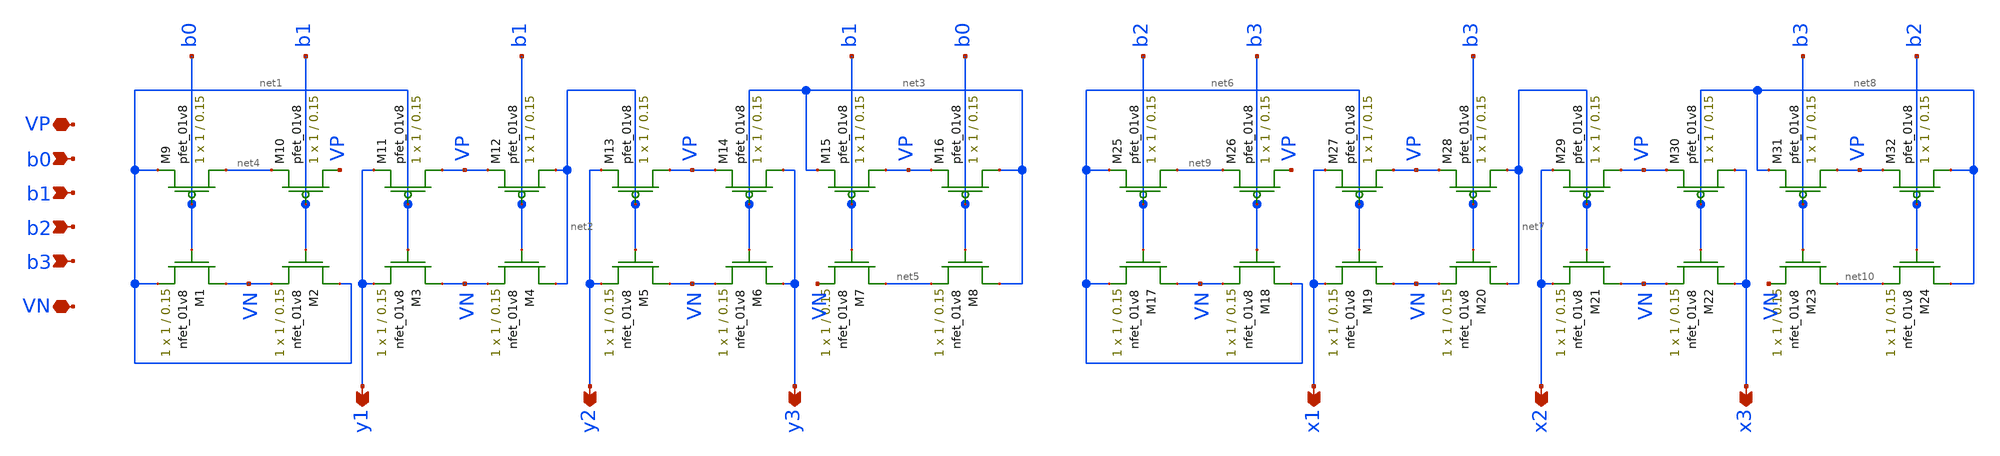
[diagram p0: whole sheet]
** sch_path: xschem/binary_decoder_4bit_lvs.sch
**.subckt binary_decoder_4bit_lvs b0 b1 b2 b3 x3 VP VN y1 y2 y3 x1 x2
*.ipin b0
*.ipin b1
*.ipin b2
*.ipin b3
*.opin x3
*.iopin VP
*.iopin VN
*.opin y1
*.opin y2
*.opin y3
*.opin x1
*.opin x2
XM1 VN b0 net1 GND sky130_fd_pr__nfet_01v8 L=0.15 W=1 nf=1 ad='int((nf+1)/2) * W/nf * 0.29' as='int((nf+2)/2) * W/nf * 0.29'
+ pd='2*int((nf+1)/2) * (W/nf + 0.29)' ps='2*int((nf+2)/2) * (W/nf + 0.29)' nrd='0.29 / W' nrs='0.29 / W'
+ sa=0 sb=0 sd=0 mult=1 m=1
XM2 net1 b1 VN GND sky130_fd_pr__nfet_01v8 L=0.15 W=1 nf=1 ad='int((nf+1)/2) * W/nf * 0.29' as='int((nf+2)/2) * W/nf * 0.29'
+ pd='2*int((nf+1)/2) * (W/nf + 0.29)' ps='2*int((nf+2)/2) * (W/nf + 0.29)' nrd='0.29 / W' nrs='0.29 / W'
+ sa=0 sb=0 sd=0 mult=1 m=1
XM3 VN net1 y1 GND sky130_fd_pr__nfet_01v8 L=0.15 W=1 nf=1 ad='int((nf+1)/2) * W/nf * 0.29' as='int((nf+2)/2) * W/nf * 0.29'
+ pd='2*int((nf+1)/2) * (W/nf + 0.29)' ps='2*int((nf+2)/2) * (W/nf + 0.29)' nrd='0.29 / W' nrs='0.29 / W'
+ sa=0 sb=0 sd=0 mult=1 m=1
XM4 net2 b1 VN GND sky130_fd_pr__nfet_01v8 L=0.15 W=1 nf=1 ad='int((nf+1)/2) * W/nf * 0.29' as='int((nf+2)/2) * W/nf * 0.29'
+ pd='2*int((nf+1)/2) * (W/nf + 0.29)' ps='2*int((nf+2)/2) * (W/nf + 0.29)' nrd='0.29 / W' nrs='0.29 / W'
+ sa=0 sb=0 sd=0 mult=1 m=1
XM5 VN net2 y2 GND sky130_fd_pr__nfet_01v8 L=0.15 W=1 nf=1 ad='int((nf+1)/2) * W/nf * 0.29' as='int((nf+2)/2) * W/nf * 0.29'
+ pd='2*int((nf+1)/2) * (W/nf + 0.29)' ps='2*int((nf+2)/2) * (W/nf + 0.29)' nrd='0.29 / W' nrs='0.29 / W'
+ sa=0 sb=0 sd=0 mult=1 m=1
XM6 y3 net3 VN GND sky130_fd_pr__nfet_01v8 L=0.15 W=1 nf=1 ad='int((nf+1)/2) * W/nf * 0.29' as='int((nf+2)/2) * W/nf * 0.29'
+ pd='2*int((nf+1)/2) * (W/nf + 0.29)' ps='2*int((nf+2)/2) * (W/nf + 0.29)' nrd='0.29 / W' nrs='0.29 / W'
+ sa=0 sb=0 sd=0 mult=1 m=1
XM7 net5 b1 VN GND sky130_fd_pr__nfet_01v8 L=0.15 W=1 nf=1 ad='int((nf+1)/2) * W/nf * 0.29' as='int((nf+2)/2) * W/nf * 0.29'
+ pd='2*int((nf+1)/2) * (W/nf + 0.29)' ps='2*int((nf+2)/2) * (W/nf + 0.29)' nrd='0.29 / W' nrs='0.29 / W'
+ sa=0 sb=0 sd=0 mult=1 m=1
XM8 net3 b0 net5 GND sky130_fd_pr__nfet_01v8 L=0.15 W=1 nf=1 ad='int((nf+1)/2) * W/nf * 0.29' as='int((nf+2)/2) * W/nf * 0.29'
+ pd='2*int((nf+1)/2) * (W/nf + 0.29)' ps='2*int((nf+2)/2) * (W/nf + 0.29)' nrd='0.29 / W' nrs='0.29 / W'
+ sa=0 sb=0 sd=0 mult=1 m=1
XM9 net4 b0 net1 VDD sky130_fd_pr__pfet_01v8 L=0.15 W=1 nf=1 ad='int((nf+1)/2) * W/nf * 0.29' as='int((nf+2)/2) * W/nf * 0.29'
+ pd='2*int((nf+1)/2) * (W/nf + 0.29)' ps='2*int((nf+2)/2) * (W/nf + 0.29)' nrd='0.29 / W' nrs='0.29 / W'
+ sa=0 sb=0 sd=0 mult=1 m=1
XM10 VP b1 net4 VDD sky130_fd_pr__pfet_01v8 L=0.15 W=1 nf=1 ad='int((nf+1)/2) * W/nf * 0.29' as='int((nf+2)/2) * W/nf * 0.29'
+ pd='2*int((nf+1)/2) * (W/nf + 0.29)' ps='2*int((nf+2)/2) * (W/nf + 0.29)' nrd='0.29 / W' nrs='0.29 / W'
+ sa=0 sb=0 sd=0 mult=1 m=1
XM11 VP net1 y1 VDD sky130_fd_pr__pfet_01v8 L=0.15 W=1 nf=1 ad='int((nf+1)/2) * W/nf * 0.29' as='int((nf+2)/2) * W/nf * 0.29'
+ pd='2*int((nf+1)/2) * (W/nf + 0.29)' ps='2*int((nf+2)/2) * (W/nf + 0.29)' nrd='0.29 / W' nrs='0.29 / W'
+ sa=0 sb=0 sd=0 mult=1 m=1
XM12 net2 b1 VP VDD sky130_fd_pr__pfet_01v8 L=0.15 W=1 nf=1 ad='int((nf+1)/2) * W/nf * 0.29' as='int((nf+2)/2) * W/nf * 0.29'
+ pd='2*int((nf+1)/2) * (W/nf + 0.29)' ps='2*int((nf+2)/2) * (W/nf + 0.29)' nrd='0.29 / W' nrs='0.29 / W'
+ sa=0 sb=0 sd=0 mult=1 m=1
XM13 VP net2 y2 VDD sky130_fd_pr__pfet_01v8 L=0.15 W=1 nf=1 ad='int((nf+1)/2) * W/nf * 0.29' as='int((nf+2)/2) * W/nf * 0.29'
+ pd='2*int((nf+1)/2) * (W/nf + 0.29)' ps='2*int((nf+2)/2) * (W/nf + 0.29)' nrd='0.29 / W' nrs='0.29 / W'
+ sa=0 sb=0 sd=0 mult=1 m=1
XM14 y3 net3 VP VDD sky130_fd_pr__pfet_01v8 L=0.15 W=1 nf=1 ad='int((nf+1)/2) * W/nf * 0.29' as='int((nf+2)/2) * W/nf * 0.29'
+ pd='2*int((nf+1)/2) * (W/nf + 0.29)' ps='2*int((nf+2)/2) * (W/nf + 0.29)' nrd='0.29 / W' nrs='0.29 / W'
+ sa=0 sb=0 sd=0 mult=1 m=1
XM15 VP b1 net3 VDD sky130_fd_pr__pfet_01v8 L=0.15 W=1 nf=1 ad='int((nf+1)/2) * W/nf * 0.29' as='int((nf+2)/2) * W/nf * 0.29'
+ pd='2*int((nf+1)/2) * (W/nf + 0.29)' ps='2*int((nf+2)/2) * (W/nf + 0.29)' nrd='0.29 / W' nrs='0.29 / W'
+ sa=0 sb=0 sd=0 mult=1 m=1
XM16 net3 b0 VP VDD sky130_fd_pr__pfet_01v8 L=0.15 W=1 nf=1 ad='int((nf+1)/2) * W/nf * 0.29' as='int((nf+2)/2) * W/nf * 0.29'
+ pd='2*int((nf+1)/2) * (W/nf + 0.29)' ps='2*int((nf+2)/2) * (W/nf + 0.29)' nrd='0.29 / W' nrs='0.29 / W'
+ sa=0 sb=0 sd=0 mult=1 m=1
XM17 VN b2 net6 GND sky130_fd_pr__nfet_01v8 L=0.15 W=1 nf=1 ad='int((nf+1)/2) * W/nf * 0.29' as='int((nf+2)/2) * W/nf * 0.29'
+ pd='2*int((nf+1)/2) * (W/nf + 0.29)' ps='2*int((nf+2)/2) * (W/nf + 0.29)' nrd='0.29 / W' nrs='0.29 / W'
+ sa=0 sb=0 sd=0 mult=1 m=1
XM18 net6 b3 VN GND sky130_fd_pr__nfet_01v8 L=0.15 W=1 nf=1 ad='int((nf+1)/2) * W/nf * 0.29' as='int((nf+2)/2) * W/nf * 0.29'
+ pd='2*int((nf+1)/2) * (W/nf + 0.29)' ps='2*int((nf+2)/2) * (W/nf + 0.29)' nrd='0.29 / W' nrs='0.29 / W'
+ sa=0 sb=0 sd=0 mult=1 m=1
XM19 VN net6 x1 GND sky130_fd_pr__nfet_01v8 L=0.15 W=1 nf=1 ad='int((nf+1)/2) * W/nf * 0.29' as='int((nf+2)/2) * W/nf * 0.29'
+ pd='2*int((nf+1)/2) * (W/nf + 0.29)' ps='2*int((nf+2)/2) * (W/nf + 0.29)' nrd='0.29 / W' nrs='0.29 / W'
+ sa=0 sb=0 sd=0 mult=1 m=1
XM20 net7 b3 VN GND sky130_fd_pr__nfet_01v8 L=0.15 W=1 nf=1 ad='int((nf+1)/2) * W/nf * 0.29' as='int((nf+2)/2) * W/nf * 0.29'
+ pd='2*int((nf+1)/2) * (W/nf + 0.29)' ps='2*int((nf+2)/2) * (W/nf + 0.29)' nrd='0.29 / W' nrs='0.29 / W'
+ sa=0 sb=0 sd=0 mult=1 m=1
XM21 VN net7 x2 GND sky130_fd_pr__nfet_01v8 L=0.15 W=1 nf=1 ad='int((nf+1)/2) * W/nf * 0.29' as='int((nf+2)/2) * W/nf * 0.29'
+ pd='2*int((nf+1)/2) * (W/nf + 0.29)' ps='2*int((nf+2)/2) * (W/nf + 0.29)' nrd='0.29 / W' nrs='0.29 / W'
+ sa=0 sb=0 sd=0 mult=1 m=1
XM22 x3 net8 VN GND sky130_fd_pr__nfet_01v8 L=0.15 W=1 nf=1 ad='int((nf+1)/2) * W/nf * 0.29' as='int((nf+2)/2) * W/nf * 0.29'
+ pd='2*int((nf+1)/2) * (W/nf + 0.29)' ps='2*int((nf+2)/2) * (W/nf + 0.29)' nrd='0.29 / W' nrs='0.29 / W'
+ sa=0 sb=0 sd=0 mult=1 m=1
XM23 net10 b3 VN GND sky130_fd_pr__nfet_01v8 L=0.15 W=1 nf=1 ad='int((nf+1)/2) * W/nf * 0.29' as='int((nf+2)/2) * W/nf * 0.29'
+ pd='2*int((nf+1)/2) * (W/nf + 0.29)' ps='2*int((nf+2)/2) * (W/nf + 0.29)' nrd='0.29 / W' nrs='0.29 / W'
+ sa=0 sb=0 sd=0 mult=1 m=1
XM24 net8 b2 net10 GND sky130_fd_pr__nfet_01v8 L=0.15 W=1 nf=1 ad='int((nf+1)/2) * W/nf * 0.29' as='int((nf+2)/2) * W/nf * 0.29'
+ pd='2*int((nf+1)/2) * (W/nf + 0.29)' ps='2*int((nf+2)/2) * (W/nf + 0.29)' nrd='0.29 / W' nrs='0.29 / W'
+ sa=0 sb=0 sd=0 mult=1 m=1
XM25 net9 b2 net6 VDD sky130_fd_pr__pfet_01v8 L=0.15 W=1 nf=1 ad='int((nf+1)/2) * W/nf * 0.29' as='int((nf+2)/2) * W/nf * 0.29'
+ pd='2*int((nf+1)/2) * (W/nf + 0.29)' ps='2*int((nf+2)/2) * (W/nf + 0.29)' nrd='0.29 / W' nrs='0.29 / W'
+ sa=0 sb=0 sd=0 mult=1 m=1
XM26 VP b3 net9 VDD sky130_fd_pr__pfet_01v8 L=0.15 W=1 nf=1 ad='int((nf+1)/2) * W/nf * 0.29' as='int((nf+2)/2) * W/nf * 0.29'
+ pd='2*int((nf+1)/2) * (W/nf + 0.29)' ps='2*int((nf+2)/2) * (W/nf + 0.29)' nrd='0.29 / W' nrs='0.29 / W'
+ sa=0 sb=0 sd=0 mult=1 m=1
XM27 VP net6 x1 VDD sky130_fd_pr__pfet_01v8 L=0.15 W=1 nf=1 ad='int((nf+1)/2) * W/nf * 0.29' as='int((nf+2)/2) * W/nf * 0.29'
+ pd='2*int((nf+1)/2) * (W/nf + 0.29)' ps='2*int((nf+2)/2) * (W/nf + 0.29)' nrd='0.29 / W' nrs='0.29 / W'
+ sa=0 sb=0 sd=0 mult=1 m=1
XM28 net7 b3 VP VDD sky130_fd_pr__pfet_01v8 L=0.15 W=1 nf=1 ad='int((nf+1)/2) * W/nf * 0.29' as='int((nf+2)/2) * W/nf * 0.29'
+ pd='2*int((nf+1)/2) * (W/nf + 0.29)' ps='2*int((nf+2)/2) * (W/nf + 0.29)' nrd='0.29 / W' nrs='0.29 / W'
+ sa=0 sb=0 sd=0 mult=1 m=1
XM29 VP net7 x2 VDD sky130_fd_pr__pfet_01v8 L=0.15 W=1 nf=1 ad='int((nf+1)/2) * W/nf * 0.29' as='int((nf+2)/2) * W/nf * 0.29'
+ pd='2*int((nf+1)/2) * (W/nf + 0.29)' ps='2*int((nf+2)/2) * (W/nf + 0.29)' nrd='0.29 / W' nrs='0.29 / W'
+ sa=0 sb=0 sd=0 mult=1 m=1
XM30 x3 net8 VP VDD sky130_fd_pr__pfet_01v8 L=0.15 W=1 nf=1 ad='int((nf+1)/2) * W/nf * 0.29' as='int((nf+2)/2) * W/nf * 0.29'
+ pd='2*int((nf+1)/2) * (W/nf + 0.29)' ps='2*int((nf+2)/2) * (W/nf + 0.29)' nrd='0.29 / W' nrs='0.29 / W'
+ sa=0 sb=0 sd=0 mult=1 m=1
XM31 VP b3 net8 VDD sky130_fd_pr__pfet_01v8 L=0.15 W=1 nf=1 ad='int((nf+1)/2) * W/nf * 0.29' as='int((nf+2)/2) * W/nf * 0.29'
+ pd='2*int((nf+1)/2) * (W/nf + 0.29)' ps='2*int((nf+2)/2) * (W/nf + 0.29)' nrd='0.29 / W' nrs='0.29 / W'
+ sa=0 sb=0 sd=0 mult=1 m=1
XM32 net8 b2 VP VDD sky130_fd_pr__pfet_01v8 L=0.15 W=1 nf=1 ad='int((nf+1)/2) * W/nf * 0.29' as='int((nf+2)/2) * W/nf * 0.29'
+ pd='2*int((nf+1)/2) * (W/nf + 0.29)' ps='2*int((nf+2)/2) * (W/nf + 0.29)' nrd='0.29 / W' nrs='0.29 / W'
+ sa=0 sb=0 sd=0 mult=1 m=1
**.ends
.end
